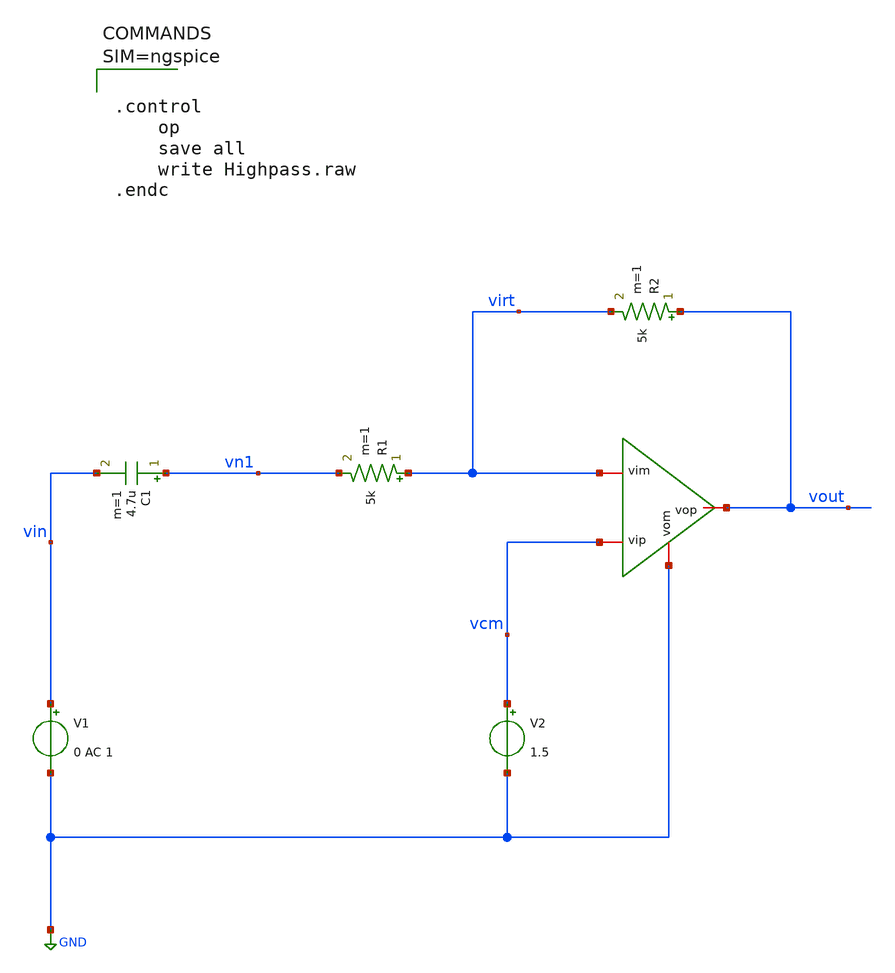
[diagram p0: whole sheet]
** sch_path: xschem/Highpass.sch
**.subckt Highpass
x1 vout vcm virt GND opam_mic1
V1 vin GND 0 AC 1
C1 vn1 vin 4.7u m=1
R1 virt vn1 5k m=1
R2 vout virt 5k m=1
V2 vcm GND 1.5
**** begin user architecture code



.control
	op
	save all
	write Highpass.raw
.endc



**** end user architecture code
**.ends

* expanding   symbol:  /home/shubham/analoginternship/xschem-proj-1/xschem/opam_mic1.sym # of pins=4
** sym_path: xschem/opam_mic1.sym
** sch_path: xschem/opam_mic1.sch
.subckt opam_mic1 vop vip vim vom
*.iopin vip
*.iopin vim
*.iopin vop
*.iopin vom
E1 vop vom vip vim 1000
.ends

.GLOBAL GND
.end
